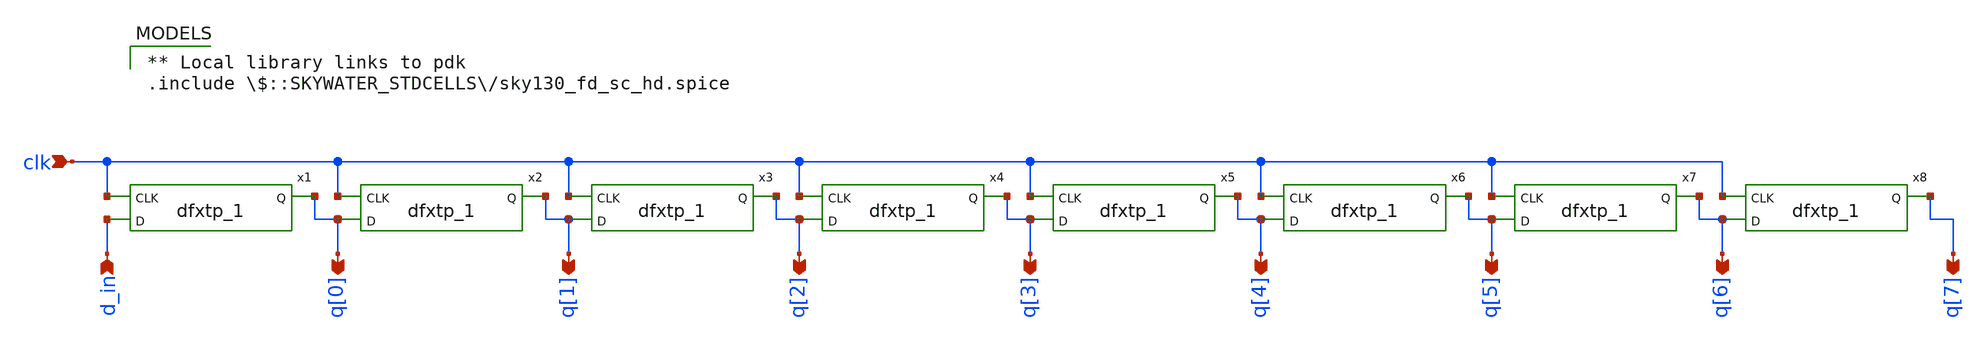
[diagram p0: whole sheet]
** sch_path: xschem/cfg_shift_register.sch
 ** Local library links to pdk
.include $::SKYWATER_STDCELLS/sky130_fd_sc_hd.spice

**.subckt cfg_shift_register clk q[0] q[1] q[2] q[3] q[4] q[5] q[6] q[7] d_in
*.ipin clk
*.opin q[0]
*.opin q[1]
*.opin q[2]
*.opin q[3]
*.opin q[4]
*.opin q[5]
*.opin q[6]
*.opin q[7]
*.ipin d_in
x1 clk d_in GND GND VDD VDD q[0] sky130_fd_sc_hd__dfxtp_1
x2 clk q[0] GND GND VDD VDD q[1] sky130_fd_sc_hd__dfxtp_1
x3 clk q[1] GND GND VDD VDD q[2] sky130_fd_sc_hd__dfxtp_1
x4 clk q[2] GND GND VDD VDD q[3] sky130_fd_sc_hd__dfxtp_1
x5 clk q[3] GND GND VDD VDD q[4] sky130_fd_sc_hd__dfxtp_1
x6 clk q[4] GND GND VDD VDD q[5] sky130_fd_sc_hd__dfxtp_1
x7 clk q[5] GND GND VDD VDD q[6] sky130_fd_sc_hd__dfxtp_1
x8 clk q[6] GND GND VDD VDD q[7] sky130_fd_sc_hd__dfxtp_1
**.ends
.end
